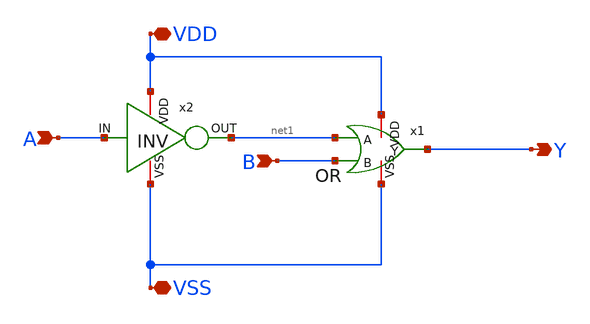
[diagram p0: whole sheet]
** sch_path: IMPLY.sch
**.subckt IMPLY A B VDD VSS Y
*.ipin A
*.ipin B
*.iopin VDD
*.iopin VSS
*.opin Y
x2 VDD net1 A VSS INV
x1 VDD net1 Y B VSS OR
**.ends

* expanding   symbol:  INV.sym # of pins=4
** sym_path: INV.sym
** sch_path: INV.sch
.subckt INV VDD OUT IN VSS
*.opin OUT
*.ipin IN
*.iopin VDD
*.iopin VSS
M2 OUT IN VDD VDD pch w=5u l=0.35u as=0 ps=0 ad=0 pd=0 m=1
M1 OUT IN VSS VSS nch w=2.5u l=0.35u as=0 ps=0 ad=0 pd=0 m=1
.ends


* expanding   symbol:  OR.sym # of pins=5
** sym_path: OR.sym
** sch_path: OR.sch
.subckt OR VDD A Y B VSS
*.iopin VDD
*.ipin A
*.ipin B
*.iopin VSS
*.opin Y
M1 net1 A VSS VSS nch w=3.5u l=0.35u as=0 ps=0 ad=0 pd=0 m=1
M2 net2 A VDD VDD pch w=3.5u l=0.35u as=0 ps=0 ad=0 pd=0 m=1
M3 net1 B net2 VDD pch w=3.5u l=0.35u as=0 ps=0 ad=0 pd=0 m=1
M4 net1 B VSS VSS nch w=3.5u l=0.35u as=0 ps=0 ad=0 pd=0 m=1
M5 Y net1 VDD VDD pch w=10u l=0.35u as=0 ps=0 ad=0 pd=0 m=1
M6 Y net1 VSS VSS nch w=5u l=0.35u as=0 ps=0 ad=0 pd=0 m=1
.ends

.end
